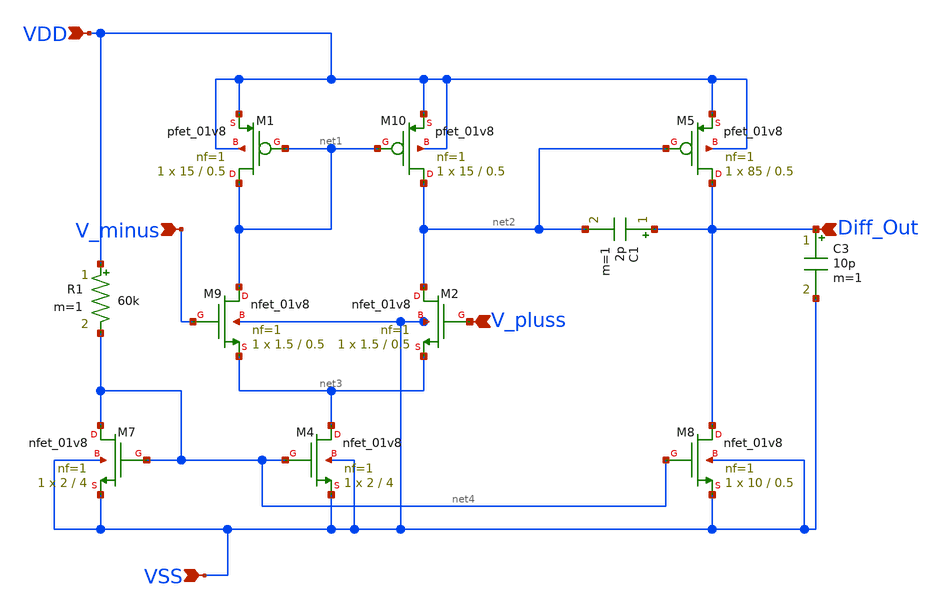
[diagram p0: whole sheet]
** sch_path: design/JNW_GR01_SKY130A/SKY_OTA.sch
**.subckt SKY_OTA VDD V_minus V_pluss VSS Diff_Out
*.ipin VDD
*.ipin V_minus
*.ipin V_pluss
*.ipin VSS
*.ipin Diff_Out
C1 Diff_Out net2 2p m=1
XM9 net1 V_minus net3 VSS sky130_fd_pr__nfet_01v8 L=0.5 W=1.5 nf=1 ad='int((nf+1)/2) * W/nf * 0.29' as='int((nf+2)/2) * W/nf * 0.29'
+ pd='2*int((nf+1)/2) * (W/nf + 0.29)' ps='2*int((nf+2)/2) * (W/nf + 0.29)' nrd='0.29 / W' nrs='0.29 / W'
+ sa=0 sb=0 sd=0 mult=1 m=1
XM10 net2 net1 VDD VDD sky130_fd_pr__pfet_01v8 L=0.5 W=15 nf=1 ad='int((nf+1)/2) * W/nf * 0.29' as='int((nf+2)/2) * W/nf * 0.29'
+ pd='2*int((nf+1)/2) * (W/nf + 0.29)' ps='2*int((nf+2)/2) * (W/nf + 0.29)' nrd='0.29 / W' nrs='0.29 / W'
+ sa=0 sb=0 sd=0 mult=1 m=1
XM2 net2 V_pluss net3 VSS sky130_fd_pr__nfet_01v8 L=0.5 W=1.5 nf=1 ad='int((nf+1)/2) * W/nf * 0.29' as='int((nf+2)/2) * W/nf * 0.29'
+ pd='2*int((nf+1)/2) * (W/nf + 0.29)' ps='2*int((nf+2)/2) * (W/nf + 0.29)' nrd='0.29 / W' nrs='0.29 / W'
+ sa=0 sb=0 sd=0 mult=1 m=1
XM1 net1 net1 VDD VDD sky130_fd_pr__pfet_01v8 L=0.5 W=15 nf=1 ad='int((nf+1)/2) * W/nf * 0.29' as='int((nf+2)/2) * W/nf * 0.29'
+ pd='2*int((nf+1)/2) * (W/nf + 0.29)' ps='2*int((nf+2)/2) * (W/nf + 0.29)' nrd='0.29 / W' nrs='0.29 / W'
+ sa=0 sb=0 sd=0 mult=1 m=1
XM4 net3 net4 VSS VSS sky130_fd_pr__nfet_01v8 L=4 W=2 nf=1 ad='int((nf+1)/2) * W/nf * 0.29' as='int((nf+2)/2) * W/nf * 0.29'
+ pd='2*int((nf+1)/2) * (W/nf + 0.29)' ps='2*int((nf+2)/2) * (W/nf + 0.29)' nrd='0.29 / W' nrs='0.29 / W'
+ sa=0 sb=0 sd=0 mult=1 m=1
XM5 Diff_Out net2 VDD VDD sky130_fd_pr__pfet_01v8 L=0.5 W=85 nf=1 ad='int((nf+1)/2) * W/nf * 0.29' as='int((nf+2)/2) * W/nf * 0.29'
+ pd='2*int((nf+1)/2) * (W/nf + 0.29)' ps='2*int((nf+2)/2) * (W/nf + 0.29)' nrd='0.29 / W' nrs='0.29 / W'
+ sa=0 sb=0 sd=0 mult=1 m=1
XM7 net4 net4 VSS VSS sky130_fd_pr__nfet_01v8 L=4 W=2 nf=1 ad='int((nf+1)/2) * W/nf * 0.29' as='int((nf+2)/2) * W/nf * 0.29'
+ pd='2*int((nf+1)/2) * (W/nf + 0.29)' ps='2*int((nf+2)/2) * (W/nf + 0.29)' nrd='0.29 / W' nrs='0.29 / W'
+ sa=0 sb=0 sd=0 mult=1 m=1
R1 VDD net4 60k m=1
XM8 Diff_Out net4 VSS VSS sky130_fd_pr__nfet_01v8 L=0.5 W=10 nf=1 ad='int((nf+1)/2) * W/nf * 0.29' as='int((nf+2)/2) * W/nf * 0.29'
+ pd='2*int((nf+1)/2) * (W/nf + 0.29)' ps='2*int((nf+2)/2) * (W/nf + 0.29)' nrd='0.29 / W' nrs='0.29 / W'
+ sa=0 sb=0 sd=0 mult=1 m=1
C3 Diff_Out VSS 10p m=1
**.ends
.end
